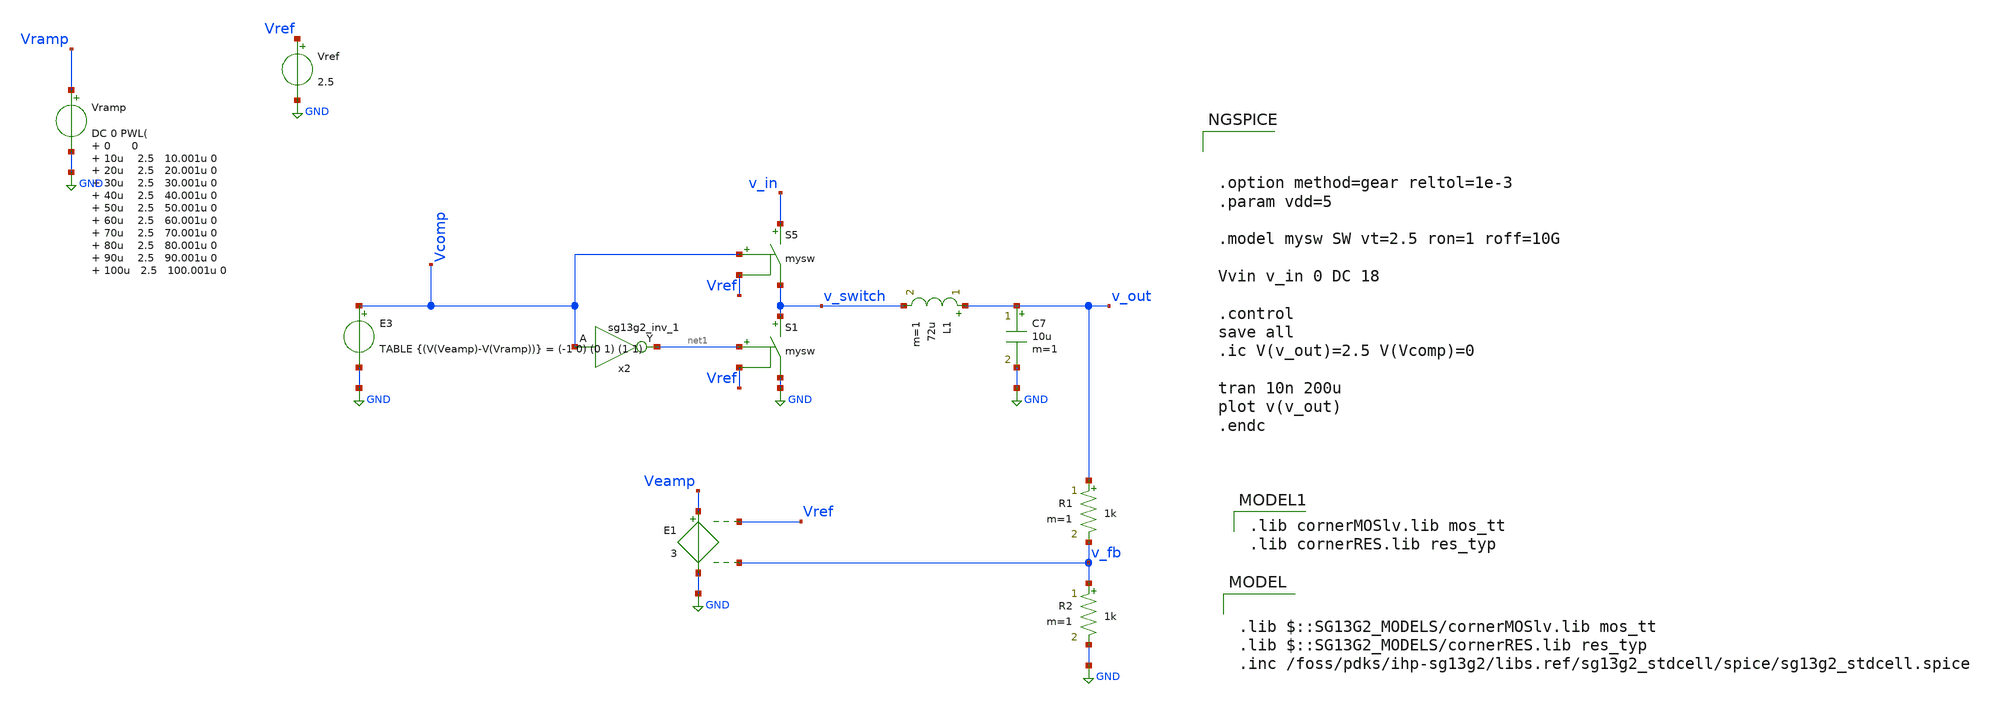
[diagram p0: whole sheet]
** sch_path: Designs/ideal_circuits/ideal_dcdc.sch
* (c) 2025 Thesis_HP, Apache-2.0 license
**.subckt ideal_dcdc
Vramp Vramp GND DC 0 PWL( 0 0 10u 2.5 10.001u 0 20u 2.5 20.001u 0 30u 2.5 30.001u 0 40u 2.5 40.001u
+ 0 50u 2.5 50.001u 0 60u 2.5 60.001u 0 70u 2.5 70.001u 0 80u 2.5 80.001u 0 90u 2.5 90.001u 0 100u 2.5
+ 100.001u 0 110u 2.5 110.001u 0 120u 2.5 120.001u 0 130u 2.5 130.001u 0 140u 2.5 140.001u 0 150u 2.5 150.001u
+ 0 160u 2.5 160.001u 0 170u 2.5 170.001u 0 180u 2.5 180.001u 0 190u 2.5 190.001u 0 200u 2.5 200.001u 0
))
S5 v_in v_switch Vcomp Vref mysw
S1 v_switch GND net1 Vref mysw
L1 v_out v_switch 72u m=1
C7 v_out GND 10u m=1
R1 v_out v_fb 1k m=1
R2 v_fb GND 1k m=1
Vref Vref GND 2.5
x2 net1 Vcomp 1.5 0 sg13g2_inv_1
E3 Vcomp GND TABLE {(V(Veamp)-V(Vramp))} = (-1 0) (0 1) (1 1)
E1 Veamp GND Vref v_fb 3
**** begin user architecture code



.option method=gear reltol=1e-3
.param vdd=5

.model mysw SW vt=2.5 ron=1 roff=10G

Vvin v_in 0 DC 18

.control
save all
.ic V(v_out)=2.5 V(Vcomp)=0

tran 10n 200u
plot v(v_out)
.endc


 .lib cornerMOSlv.lib mos_tt
.lib cornerRES.lib res_typ


.lib $::SG13G2_MODELS/cornerMOSlv.lib mos_tt
.lib $::SG13G2_MODELS/cornerRES.lib res_typ
.inc /foss/pdks/ihp-sg13g2/libs.ref/sg13g2_stdcell/spice/sg13g2_stdcell.spice

**** end user architecture code
**.ends

* expanding   symbol:  sg13g2_stdcells/sg13g2_inv_1.sym # of pins=2
** sym_path: sg13g2_stdcells/sg13g2_inv_1.sym
** sch_path: sg13g2_stdcells/sg13g2_inv_1.sch
.subckt sg13g2_inv_1 Y A VDD VSS
*.opin Y
*.ipin A
*.iopin VDD
*.iopin VSS
XM1 Y A VSS VSS sg13_lv_nmos w=740.00n l=130.00n ng=1 m=1 mm_ok=1
XM2 Y A VDD VDD sg13_lv_pmos w=1.12u l=130.00n ng=1 m=1 mm_ok=1
.ends

.GLOBAL GND
.end
